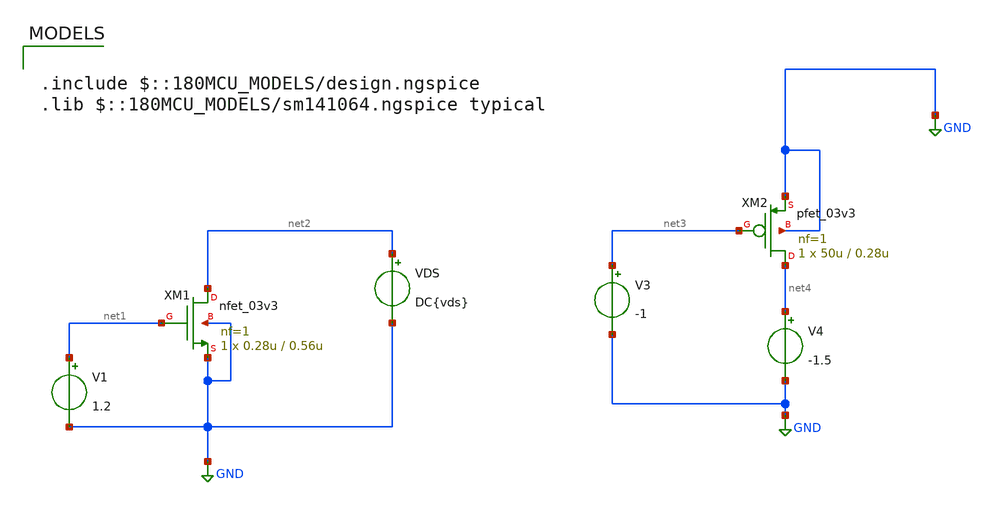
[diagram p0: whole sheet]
** sch_path: DAC_PAKISTAN_01/Pakistan1_Xschem/DC_trans.sch
**.subckt DC_trans
XM1 net2 net1 GND GND nfet_03v3 L=0.56u W=0.28u nf=1 ad='int((nf+1)/2) * W/nf * 0.18u' as='int((nf+2)/2) * W/nf * 0.18u'
+ pd='2*int((nf+1)/2) * (W/nf + 0.18u)' ps='2*int((nf+2)/2) * (W/nf + 0.18u)' nrd='0.18u / W' nrs='0.18u / W'
+ sa=0 sb=0 sd=0 m=1
V1 net1 GND 1.2
VDS net2 GND DC{vds}
XM2 net4 net3 GND GND pfet_03v3 L=0.28u W=50u nf=1 ad='int((nf+1)/2) * W/nf * 0.18u' as='int((nf+2)/2) * W/nf * 0.18u'
+ pd='2*int((nf+1)/2) * (W/nf + 0.18u)' ps='2*int((nf+2)/2) * (W/nf + 0.18u)' nrd='0.18u / W' nrs='0.18u / W'
+ sa=0 sb=0 sd=0 m=1
V3 net3 GND -1
V4 net4 GND -1.5
**** begin user architecture code

.include $::180MCU_MODELS/design.ngspice
.lib $::180MCU_MODELS/sm141064.ngspice typical




*Parameters
.param vds = 3.3

.options TEMP = 50.0


*Data to save
.save all  @M.xm1.m0[id]  @M.xm2.m0[id]  @M.xm1.m0[vds]  @M.xm1.m0[vgs]  @M.xm1.m0[vth]  @M.xm1.m0[cgg]  @M.xm1.m0[cgs]  @M.xm1.m0[gds]  @M.xm1.m0[gm]

*Simulation
.control

dc VDS 0 3.3 0.01
setplot dc1
*plot @M.xm1.m0[id] ylabel Id xlabel Vds
set filetype = binary
write DC_trans.raw

reset
dc V1 0 3.3 0.01
setplot dc2
*plot @M.xm1.m0[id] ylabel Id xlabel Vgs
set filetype = binary
write DC_trans2.raw

reset
op
save all
set filetype = binary
write nmos_char_dc.raw

.endc
.end


**** end user architecture code
**.ends
.GLOBAL GND
.end
